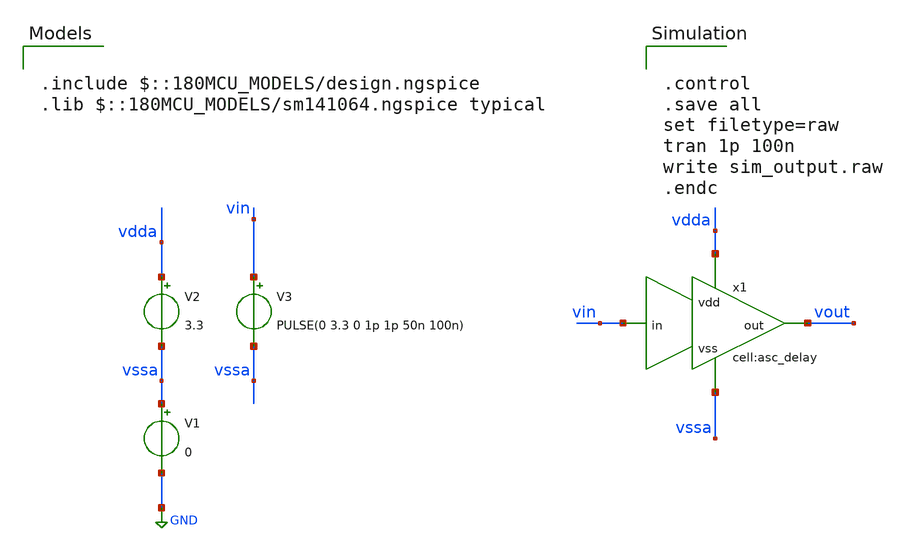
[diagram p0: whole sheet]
** sch_path: designs/libs/xp_tb_analog/tb_asc_delay/tb_asc_delay.sch
**.subckt tb_asc_delay
V1 vssa GND 0
V2 vdda vssa 3.3
V3 vin vssa PULSE(0 3.3 0 1p 1p 50n 100n)
x1 vin vssa vout vdda asc_delay
**** begin user architecture code

.include $::180MCU_MODELS/design.ngspice
.lib $::180MCU_MODELS/sm141064.ngspice typical



.control
.save all
set filetype=raw
tran 1p 100n
write sim_output.raw
.endc


**** end user architecture code
**.ends
.GLOBAL GND
.end
